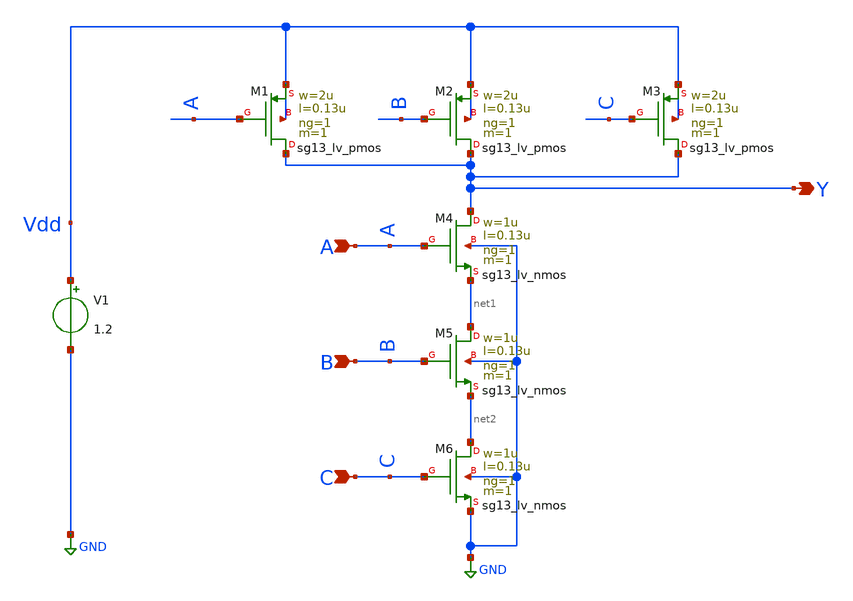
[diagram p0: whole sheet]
** sch_path: Team 1 Design/design_data/xschem/3_Input_NAND/3NAND.sch
**.subckt 3NAND A B C Y
*.ipin A
*.ipin B
*.ipin C
*.opin Y
XM1 Y A Vdd Vdd sg13_lv_pmos w=2u l=0.13u ng=1 m=1 mm_ok=1
XM2 Y B Vdd Vdd sg13_lv_pmos w=2u l=0.13u ng=1 m=1 mm_ok=1
XM3 Y C Vdd Vdd sg13_lv_pmos w=2u l=0.13u ng=1 m=1 mm_ok=1
XM4 Y A net1 GND sg13_lv_nmos w=1u l=0.13u ng=1 m=1 mm_ok=1
XM5 net1 B net2 GND sg13_lv_nmos w=1u l=0.13u ng=1 m=1 mm_ok=1
XM6 net2 C GND GND sg13_lv_nmos w=1u l=0.13u ng=1 m=1 mm_ok=1
V1 Vdd GND 1.2
**.ends
.GLOBAL GND
.end
